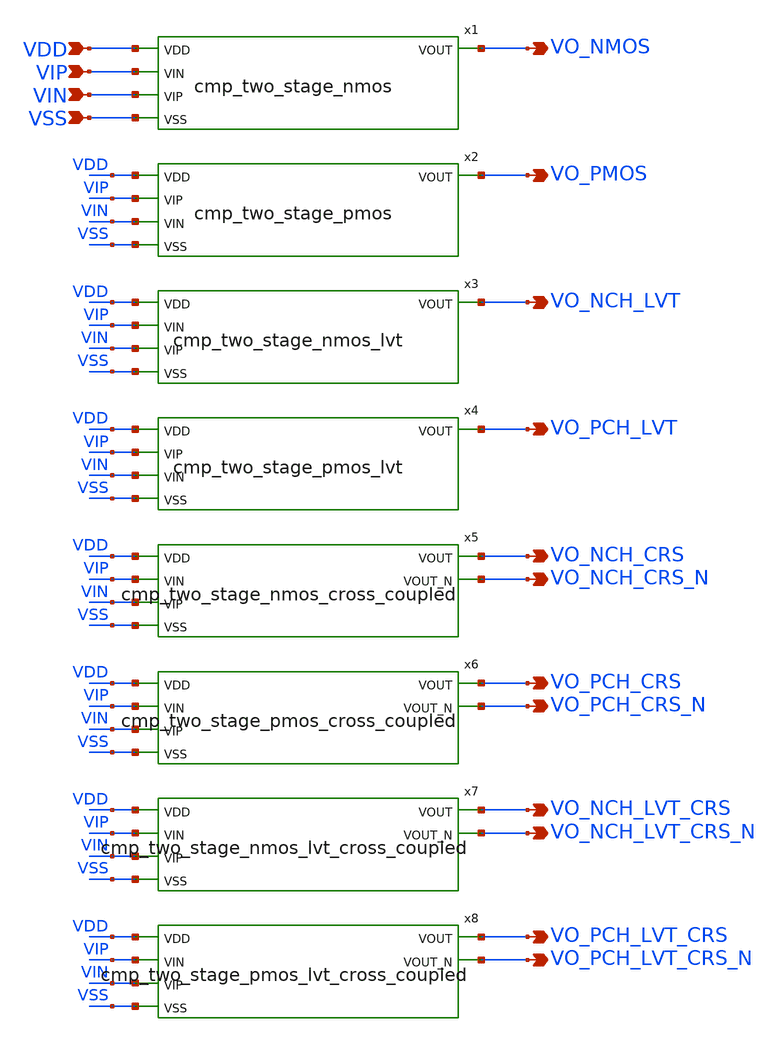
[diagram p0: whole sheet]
** sch_path: design/LELO_TORD_SKY130A/TB_cmp_gain.sch
**.subckt TB_cmp_gain VO_NMOS VDD VIP VIN VSS VO_PMOS VO_NCH_LVT VO_PCH_LVT VO_NCH_CRS VO_PCH_CRS
*+ VO_NCH_CRS_N VO_PCH_CRS_N VO_NCH_LVT_CRS VO_NCH_LVT_CRS_N VO_PCH_LVT_CRS VO_PCH_LVT_CRS_N
*.opin VO_NMOS
*.ipin VDD
*.ipin VIP
*.ipin VIN
*.ipin VSS
*.opin VO_PMOS
*.opin VO_NCH_LVT
*.opin VO_PCH_LVT
*.opin VO_NCH_CRS
*.opin VO_PCH_CRS
*.opin VO_NCH_CRS_N
*.opin VO_PCH_CRS_N
*.opin VO_NCH_LVT_CRS
*.opin VO_NCH_LVT_CRS_N
*.opin VO_PCH_LVT_CRS
*.opin VO_PCH_LVT_CRS_N
x1 VDD VO_NMOS VIP VIN VSS cmp_two_stage_nmos
x2 VDD VIP VIN VO_PMOS VSS cmp_two_stage_pmos
x3 VDD VO_NCH_LVT VIP VIN VSS cmp_two_stage_nmos_lvt
x4 VDD VIP VIN VO_PCH_LVT VSS cmp_two_stage_pmos_lvt
x5 VDD VO_NCH_CRS VIP VIN VO_NCH_CRS_N VSS cmp_two_stage_nmos_cross_coupled
x8 VDD VO_PCH_LVT_CRS VO_PCH_LVT_CRS_N VIP VIN VSS cmp_two_stage_pmos_lvt_cross_coupled
x6 VDD VO_PCH_CRS VO_PCH_CRS_N VIP VIN VSS cmp_two_stage_pmos_cross_coupled
x7 VDD VO_NCH_LVT_CRS VIP VIN VO_NCH_LVT_CRS_N VSS cmp_two_stage_nmos_lvt_cross_coupled
**.ends
.end
